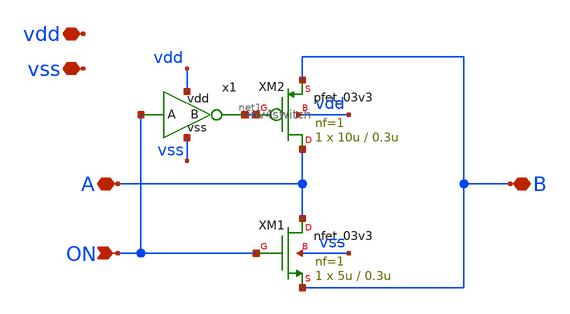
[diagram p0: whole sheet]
** sch_path: General/ADC/switching/spst.sch
**.subckt spst ON vdd vss A B
*.ipin ON
*.iopin vdd
*.iopin vss
*.iopin A
*.iopin B
XM1 A ON B vss nfet_03v3 L=0.3u W=5u nf=1 ad='int((nf+1)/2) * W/nf * 0.18u' as='int((nf+2)/2) * W/nf * 0.18u'
+ pd='2*int((nf+1)/2) * (W/nf + 0.18u)' ps='2*int((nf+2)/2) * (W/nf + 0.18u)' nrd='0.18u / W' nrs='0.18u / W'
+ sa=0 sb=0 sd=0 m=1
XM2 A net1 B vdd pfet_03v3 L=0.3u W=10u nf=1 ad='int((nf+1)/2) * W/nf * 0.18u' as='int((nf+2)/2) * W/nf * 0.18u'
+ pd='2*int((nf+1)/2) * (W/nf + 0.18u)' ps='2*int((nf+2)/2) * (W/nf + 0.18u)' nrd='0.18u / W' nrs='0.18u / W'
+ sa=0 sb=0 sd=0 m=1
x1 net1 ON vdd vss inv4switch
**.ends

* expanding   symbol:  adc/switching/inv4switch.sym # of pins=4
** sym_path: General/ADC/switching/inv4switch.sym
** sch_path: General/ADC/switching/inv4switch.sch
.subckt inv4switch B A vdd vss
*.ipin A
*.opin B
*.iopin vdd
*.iopin vss
XM1 B A vss vss nfet_03v3 L=0.3u W=1u nf=1 ad='int((nf+1)/2) * W/nf * 0.18u' as='int((nf+2)/2) * W/nf * 0.18u'
+ pd='2*int((nf+1)/2) * (W/nf + 0.18u)' ps='2*int((nf+2)/2) * (W/nf + 0.18u)' nrd='0.18u / W' nrs='0.18u / W'
+ sa=0 sb=0 sd=0 m=1
XM2 B A vdd vdd pfet_03v3 L=0.3u W=2u nf=1 ad='int((nf+1)/2) * W/nf * 0.18u' as='int((nf+2)/2) * W/nf * 0.18u'
+ pd='2*int((nf+1)/2) * (W/nf + 0.18u)' ps='2*int((nf+2)/2) * (W/nf + 0.18u)' nrd='0.18u / W' nrs='0.18u / W'
+ sa=0 sb=0 sd=0 m=1
.ends

.end
